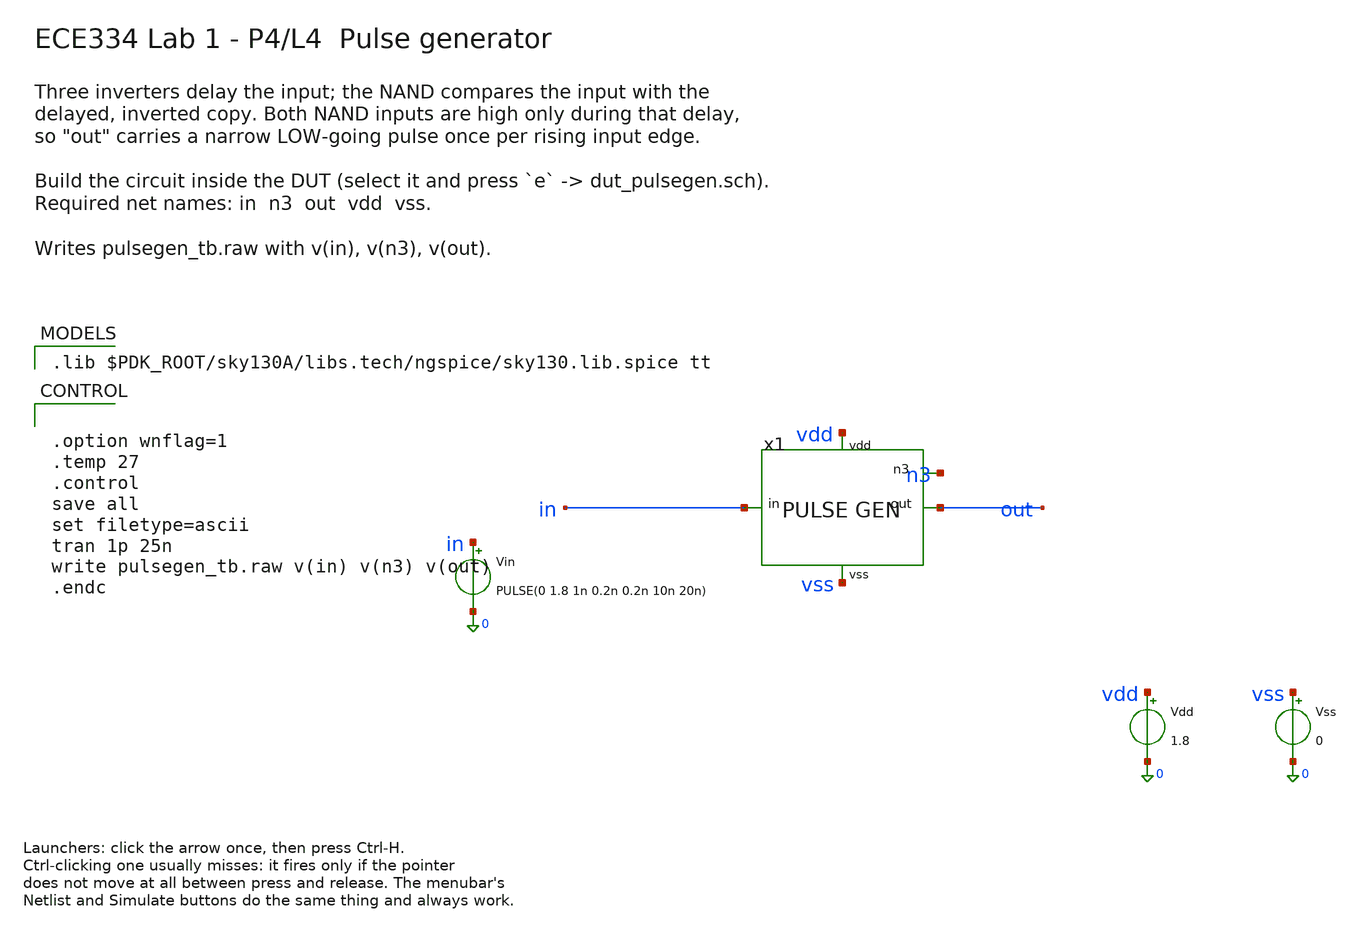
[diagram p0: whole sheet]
** sch_path: lab1_spice/xschem/pulsegen_tb.sch
**.subckt pulsegen_tb
Vin in 0 PULSE(0 1.8 1n 0.2n 0.2n 10n 20n)
x1 in n3 out vdd vss dut_pulsegen
Vdd vdd 0 1.8
Vss vss 0 0
**** begin user architecture code

.lib $PDK_ROOT/sky130A/libs.tech/ngspice/sky130.lib.spice tt



.option wnflag=1
.temp 27
.control
save all
set filetype=ascii
tran 1p 25n
write pulsegen_tb.raw v(in) v(n3) v(out)
.endc


**** end user architecture code
**.ends

* expanding   symbol:  dut_pulsegen.sym # of pins=5
** sym_path: lab1_spice/xschem/dut_pulsegen.sym
** sch_path: lab1_spice/xschem/dut_pulsegen.sch
.subckt dut_pulsegen in n3 out vdd vss
*.ipin in
*.opin n3
*.opin out
*.iopin vdd
*.iopin vss
.ends

.end
